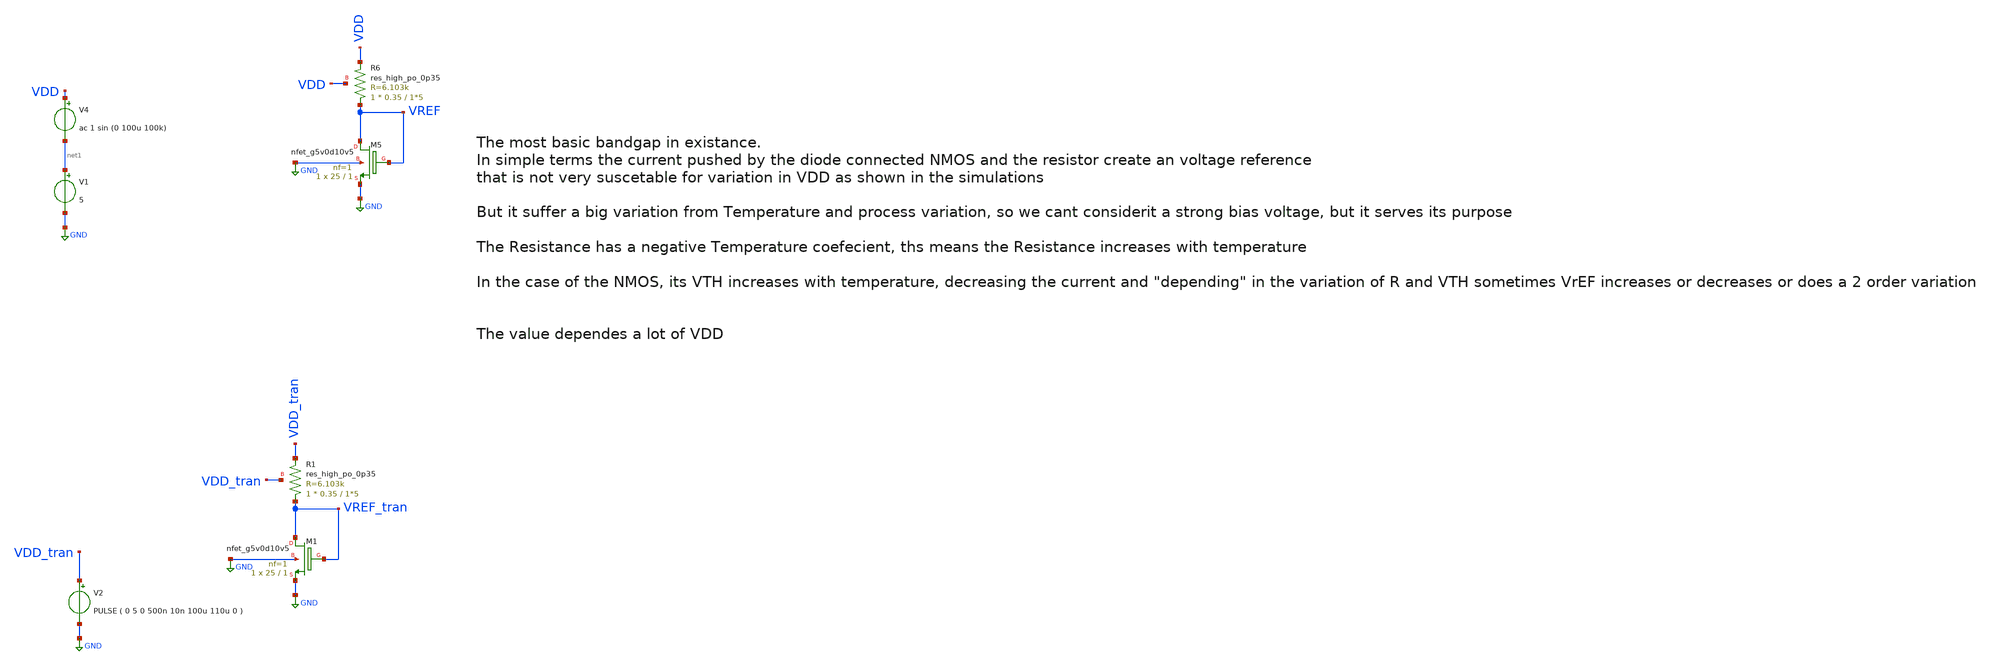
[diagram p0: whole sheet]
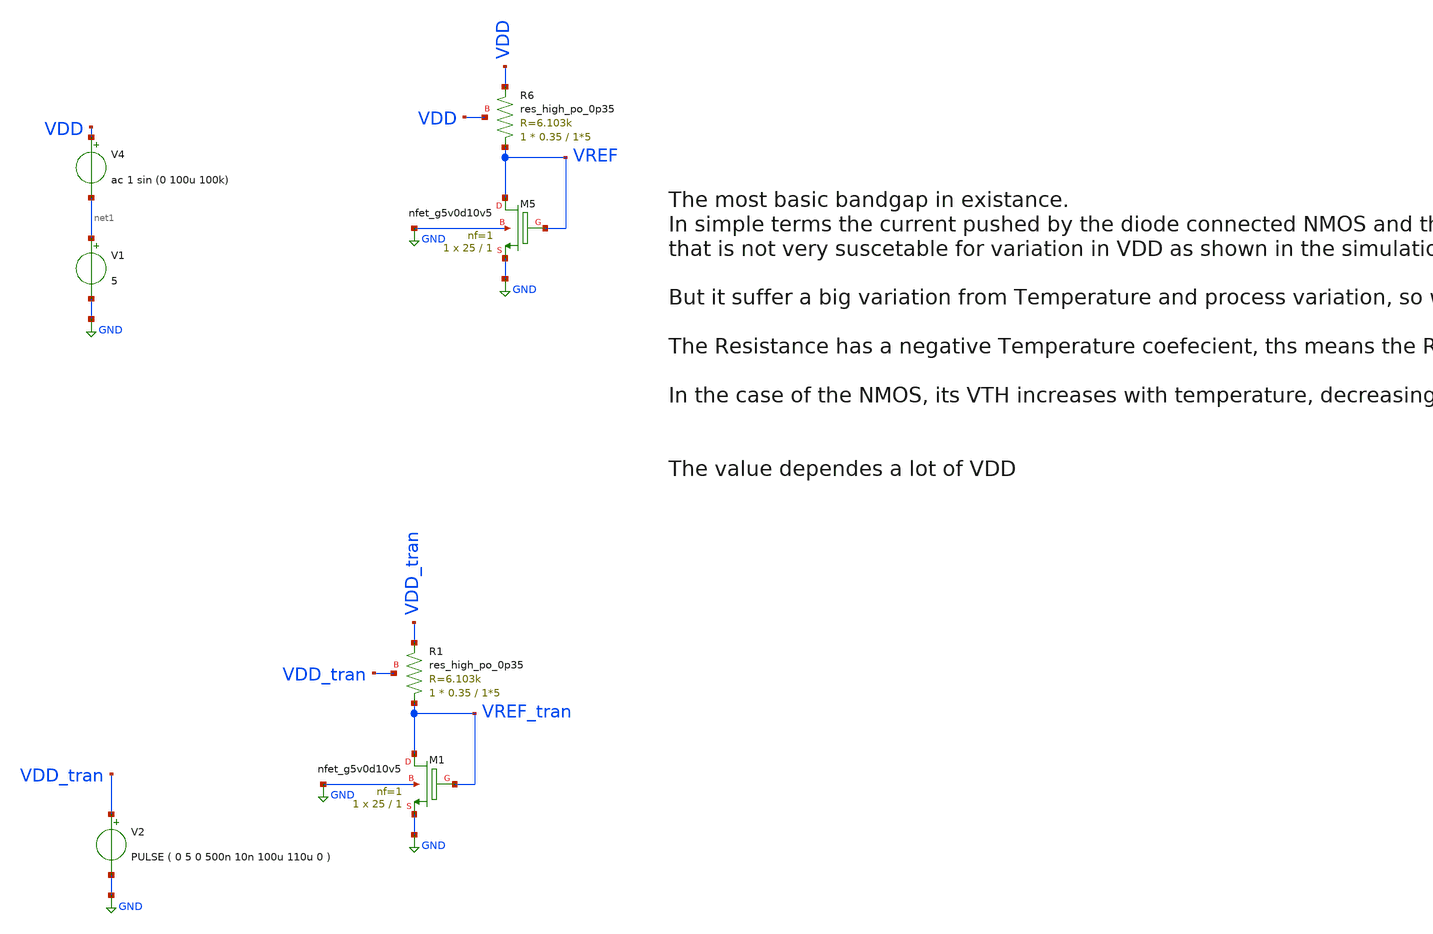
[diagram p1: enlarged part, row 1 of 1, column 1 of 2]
** sch_path: old stuff/bandgaps/resistive-NMOS_very_simple/bandgap.sch
**.subckt bandgap
V1 net1 GND 5
V2 VDD_tran GND PULSE ( 0 5 0 500n 10n 100u 110u 0 )
XM5 VREF VREF GND GND sky130_fd_pr__nfet_g5v0d10v5 L=1 W=25 nf=1 ad='int((1 + 1)/2) * 25 / 1 * 0.29'
+ as='int((1 + 2)/2) * 25 / 1 * 0.29' pd='2*int((1 + 1)/2) * (25 / 1 + 0.29)' ps='2*int((1 + 2)/2) * (25 / 1 + 0.29)'
+ nrd='0.29 / 25 ' nrs='0.29 / 25 ' sa=0 sb=0 sd=0 mult=1 m=1
V4 VDD net1 ac 1 sin (0 100u 100k)
XR6 VREF VDD VDD sky130_fd_pr__res_high_po_0p35 L=1*5 mult=1 m=1
XM1 VREF_tran VREF_tran GND GND sky130_fd_pr__nfet_g5v0d10v5 L=1 W=25 nf=1 ad='int((1 + 1)/2) * 25 / 1 * 0.29'
+ as='int((1 + 2)/2) * 25 / 1 * 0.29' pd='2*int((1 + 1)/2) * (25 / 1 + 0.29)' ps='2*int((1 + 2)/2) * (25 / 1 + 0.29)'
+ nrd='0.29 / 25 ' nrs='0.29 / 25 ' sa=0 sb=0 sd=0 mult=1 m=1
XR1 VREF_tran VDD_tran VDD_tran sky130_fd_pr__res_high_po_0p35 L=1*5 mult=1 m=1
**** begin user architecture code

**************************************************************
**************************************************************
**************************************************************
**************************************************************
**************************************************************
*LIBs*********************************************************
**************************************************************
**************************************************************
**************************************************************
**************************************************************
**************************************************************
*.lib $::SKYWATER_MODELS/sky130.lib.spice tt
* chose the corners in the corner file
* tt_mm for mismatch
* ss ff sf fs standart corners
* ll hh lh hl capacitor and resistors corners
* mc for total process variation including corners
**************************************************************
**************************************************************
**************************************************************
**************************************************************
**************************************************************
*Corners/montecarlo options***********************************
**************************************************************
**************************************************************
**************************************************************
**************************************************************
**************************************************************
.TEMP 27
**************************************************************
**************************************************************
**************************************************************
**************************************************************
*SIMULATION and Plots*****************************************
**************************************************************
**************************************************************
**************************************************************
**************************************************************
.control
save all
dc TEMP -20 140 0.01
plot v(VREF)
tran 10ns 1us
plot v(VREF_tran)
ac dec 20 1 1000G
plot db(v(VREF))

.endc

.lib $::SKYWATER_MODELS/sky130.lib.spice tt
**** end user architecture code
**.ends
.GLOBAL GND
.end
